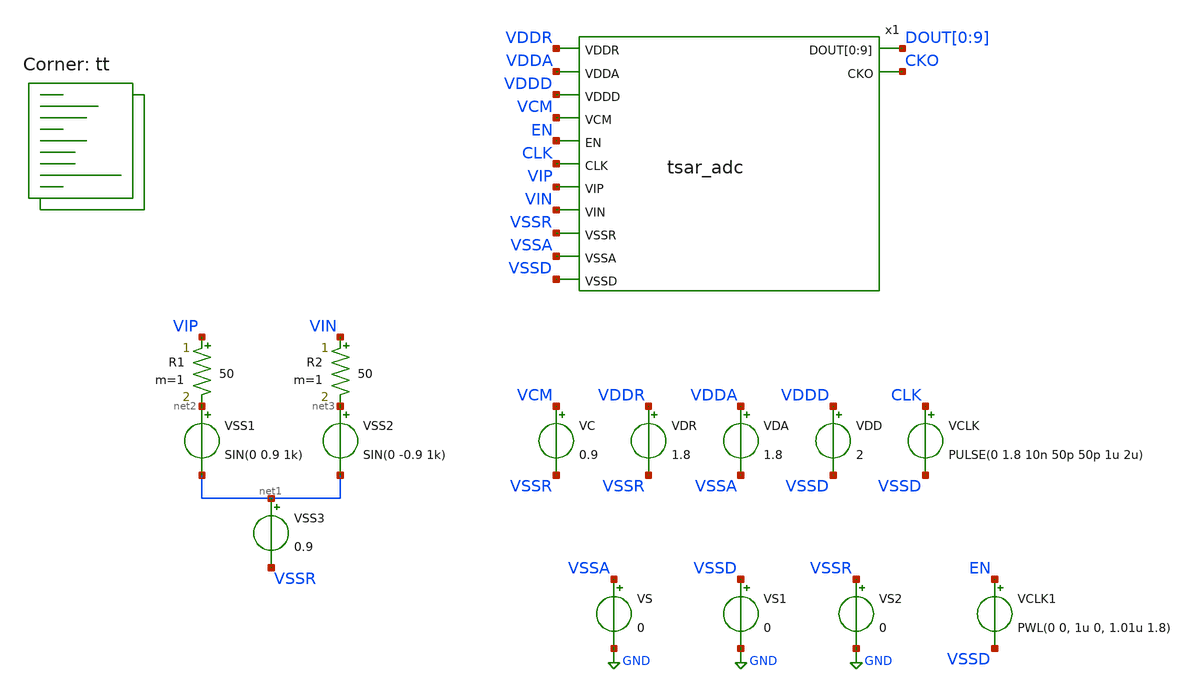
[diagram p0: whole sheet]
** sch_path: xschem/adc_tb.sch
**.subckt adc_tb
VS VSSA GND 0
VDA VDDA VSSA 1.8
VDD VDDD VSSD 2
VC VCM VSSR 0.9
VSS1 net2 net1 SIN(0 0.9 1k)
VSS2 net3 net1 SIN(0 -0.9 1k)
VSS3 net1 VSSR 0.9
VCLK CLK VSSD PULSE(0 1.8 10n 50p 50p 1u 2u)
x1 VDDR VDDA VDDD VCM EN CLK VIP VIN VSSR VSSA VSSD DOUT[0] DOUT[1] DOUT[2] DOUT[3] DOUT[4] DOUT[5]
+ DOUT[6] DOUT[7] DOUT[8] DOUT[9] CKO tsar_adc
R1 VIP net2 50 m=1
R2 VIN net3 50 m=1
VS1 VSSD GND 0
VS2 VSSR GND 0
VDR VDDR VSSR 1.8
VCLK1 EN VSSD PWL(0 0, 1u 0, 1.01u 1.8)
**** begin user architecture code

** opencircuitdesign pdks install
* .lib $::SKYWATER_MODELS/sky130.lib.spice tt
.include /usr/local/share/pdk/sky130A/libs.ref/sky130_fd_sc_hd/spice/sky130_fd_sc_hd.spice



.option wnflag=0
.option savecurrents
.options acct list
.options method=trapezoid
.options reltol=1e-2 abstol=1e-4
.options maxstep=100n
.options minbreak=10n
.options solver=iterative
.control
global netlist_dir .
set wr_singlescale
save  clk  vip  vin  x1.x1.vcp  x1.x1.vcn  x1.comp_p  x1.comp_n  x1.clks  x1.clksb  'dout[0]'  'dout[1]'
+  'dout[2]'  'dout[3]'  'dout[4]'  'dout[5]'  'dout[6]'  'dout[7]'  'dout[8]'  'dout[9]'  'x1.cf[0]' 
+ 'x1.cf[1]'  'x1.cf[2]'  'x1.cf[3]'  'x1.cf[4]'  'x1.cf[5]'  'x1.cf[6]'  'x1.cf[7]'  'x1.cf[8]'  'x1.cf[9]'
+  cko
tran 100n 0.5m
remzerovec
write adc_tb.raw
quit 0
.endc

.lib $::SKYWATER_MODELS/sky130.lib.spice tt
**** end user architecture code
**.ends
.GLOBAL GND
.end
